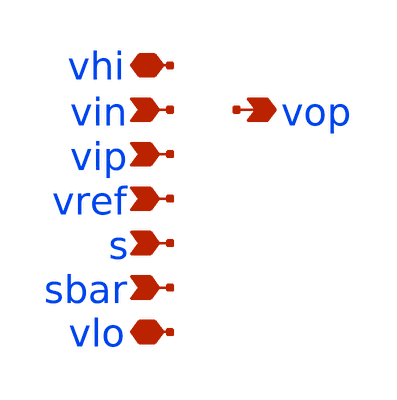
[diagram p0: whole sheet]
** sch_path: xschem/i_type_ota_gb_rp_gp_PEX.sch
**.subckt i_type_ota_gb_rp_gp_PEX vip vin vop vhi vlo vref s sbar
*.ipin vip
*.ipin vin
*.opin vop
*.iopin vhi
*.iopin vlo
*.ipin vref
*.ipin s
*.ipin sbar
**** begin user architecture code

* NGSPICE file created from cmota_1_flat.ext - technology: sky130A

.subckt cmota_gb_rp_gp VHI VLO VREF VIP VIN VOP S SBAR


X0 VLO a_n2179_n5512# a_n2179_n5512# VLO sky130_fd_pr__nfet_01v8 ad=0p pd=0u as=0p ps=0u w=1e+07u
+ l=300000u
X1 VLO VLO VLO VLO sky130_fd_pr__nfet_01v8 ad=0p pd=0u as=0p ps=0u w=1e+07u l=300000u
X2 a_n999_n4100# VIP a_n644_n3012# VLO sky130_fd_pr__nfet_01v8_lvt ad=0p pd=0u as=0p ps=0u
+ w=2.5e+06u l=150000u
X3 VLO VREF_GATED a_n999_n4100# VLO sky130_fd_pr__nfet_01v8 ad=0p pd=0u as=0p ps=0u w=1e+07u
+ l=2e+06u
X4 VREF_GATED S a_n3594_n6504# VLO sky130_fd_pr__nfet_01v8 ad=0p pd=0u as=0p ps=0u w=2.5e+06u
+ l=150000u
X5 VLO VREF_GATED a_n999_n4100# VLO sky130_fd_pr__nfet_01v8 ad=0p pd=0u as=0p ps=0u w=1e+07u
+ l=2e+06u
X6 a_n999_n4100# VIP a_n644_n3012# VLO sky130_fd_pr__nfet_01v8_lvt ad=0p pd=0u as=0p ps=0u
+ w=2.5e+06u l=150000u
X7 a_n3594_n6504# SBAR VLO VLO sky130_fd_pr__nfet_01v8 ad=0p pd=0u as=0p ps=0u w=2.5e+06u l=150000u
X8 VHI a_n644_n3012# VOP VHI sky130_fd_pr__pfet_01v8 ad=0p pd=0u as=0p ps=0u w=1e+07u l=300000u
X9 VLO VLO a_n999_n4100# VLO sky130_fd_pr__nfet_01v8_lvt ad=0p pd=0u as=0p ps=0u w=2.5e+06u
+ l=150000u
X10 VOP a_n644_n3012# VHI VHI sky130_fd_pr__pfet_01v8 ad=0p pd=0u as=0p ps=0u w=1e+07u l=300000u
X11 VLO VLO VLO VLO sky130_fd_pr__nfet_01v8_lvt ad=0p pd=0u as=0p ps=0u w=2.5e+06u l=150000u
X12 VLO VLO VLO VLO sky130_fd_pr__nfet_01v8 ad=0p pd=0u as=0p ps=0u w=1e+07u l=300000u
X13 VOP a_n2179_n5512# VLO VLO sky130_fd_pr__nfet_01v8 ad=0p pd=0u as=0p ps=0u w=1e+07u l=300000u
X14 VHI a_n644_n3012# VOP VHI sky130_fd_pr__pfet_01v8 ad=0p pd=0u as=0p ps=0u w=1e+07u l=300000u
X15 VLO a_n2179_n5512# VOP VLO sky130_fd_pr__nfet_01v8 ad=0p pd=0u as=0p ps=0u w=1e+07u l=300000u
X16 VLO VHI sky130_fd_pr__cap_mim_m3_2 l=3.1e+07u w=1.3e+07u
X17 VOP a_n644_n3012# VHI VHI sky130_fd_pr__pfet_01v8 ad=0p pd=0u as=0p ps=0u w=1e+07u l=300000u
X18 VLO a_n2179_n5512# a_n2179_n5512# VLO sky130_fd_pr__nfet_01v8 ad=0p pd=0u as=0p ps=0u w=1e+07u
+ l=300000u
X19 VHI a_n1942_n3012# a_n1942_n3012# VHI sky130_fd_pr__pfet_01v8 ad=0p pd=0u as=0p ps=0u w=1e+07u
+ l=300000u
X20 VLO VLO VLO VLO sky130_fd_pr__nfet_01v8 ad=0p pd=0u as=0p ps=0u w=1e+07u l=300000u
X21 a_n2179_n5512# a_n2179_n5512# VLO VLO sky130_fd_pr__nfet_01v8 ad=0p pd=0u as=0p ps=0u w=1e+07u
+ l=300000u
X22 VHI a_n1942_n3012# a_n1942_n3012# VHI sky130_fd_pr__pfet_01v8 ad=0p pd=0u as=0p ps=0u w=1e+07u
+ l=300000u
X23 a_n1942_n3012# a_n1942_n3012# VHI VHI sky130_fd_pr__pfet_01v8 ad=0p pd=0u as=0p ps=0u w=1e+07u
+ l=300000u
X24 a_n1942_n3012# VIN a_n999_n4100# VLO sky130_fd_pr__nfet_01v8_lvt ad=0p pd=0u as=0p ps=0u
+ w=2.5e+06u l=150000u
X25 a_127_n2915# a_n1942_n3012# VHI VHI sky130_fd_pr__pfet_01v8 ad=0p pd=0u as=0p ps=0u w=1e+07u
+ l=300000u
X26 a_n2179_n5512# a_n2179_n5512# VLO VLO sky130_fd_pr__nfet_01v8 ad=0p pd=0u as=0p ps=0u w=1e+07u
+ l=300000u
X27 a_n999_n4100# VIN a_n1942_n3012# VLO sky130_fd_pr__nfet_01v8_lvt ad=0p pd=0u as=0p ps=0u
+ w=2.5e+06u l=150000u
X28 a_n2179_n5512# a_n1942_n3012# VHI VHI sky130_fd_pr__pfet_01v8 ad=0p pd=0u as=0p ps=0u w=1e+07u
+ l=300000u
X29 VHI a_n1942_n3012# a_n2179_n5512# VHI sky130_fd_pr__pfet_01v8 ad=0p pd=0u as=0p ps=0u w=1e+07u
+ l=300000u
X30 a_n644_n3012# a_n644_n3012# VHI VHI sky130_fd_pr__pfet_01v8 ad=0p pd=0u as=0p ps=0u w=1e+07u
+ l=300000u
X31 VHI a_n644_n3012# a_n644_n3012# VHI sky130_fd_pr__pfet_01v8 ad=0p pd=0u as=0p ps=0u w=1e+07u
+ l=300000u
X32 a_n644_n3012# VIP a_n999_n4100# VLO sky130_fd_pr__nfet_01v8_lvt ad=0p pd=0u as=0p ps=0u
+ w=2.5e+06u l=150000u
X33 VLO VREF_GATED sky130_fd_pr__cap_mim_m3_1 l=2.7e+07u w=5.5e+06u
X34 a_n999_n4100# VIN a_n1942_n3012# VLO sky130_fd_pr__nfet_01v8_lvt ad=0p pd=0u as=0p ps=0u
+ w=2.5e+06u l=150000u
X35 a_n1942_n3012# VIN a_n999_n4100# VLO sky130_fd_pr__nfet_01v8_lvt ad=0p pd=0u as=0p ps=0u
+ w=2.5e+06u l=150000u
X36 VLO SBAR a_n3594_n6504# VLO sky130_fd_pr__nfet_01v8 ad=0p pd=0u as=0p ps=0u w=2.5e+06u l=150000u
X37 a_n644_n3012# VIP a_n999_n4100# VLO sky130_fd_pr__nfet_01v8_lvt ad=0p pd=0u as=0p ps=0u
+ w=2.5e+06u l=150000u
X38 a_n2179_n5512# VHI VHI VHI sky130_fd_pr__pfet_01v8 ad=0p pd=0u as=0p ps=0u w=1e+07u l=300000u
X39 VREF_GATED VLO sky130_fd_pr__cap_mim_m3_2 l=2.7e+07u w=5.5e+06u
X40 VHI a_n644_n3012# a_n1942_n3012# VHI sky130_fd_pr__pfet_01v8 ad=0p pd=0u as=0p ps=0u w=1e+07u
+ l=300000u
X41 a_n644_n3012# a_n1942_n3012# VHI VHI sky130_fd_pr__pfet_01v8 ad=0p pd=0u as=0p ps=0u w=1e+07u
+ l=300000u
X42 VHI a_n1942_n3012# a_n644_n3012# VHI sky130_fd_pr__pfet_01v8 ad=0p pd=0u as=0p ps=0u w=1e+07u
+ l=300000u
X43 VHI VHI VOP VHI sky130_fd_pr__pfet_01v8 ad=0p pd=0u as=0p ps=0u w=1e+07u l=300000u
X44 a_n999_n4100# VIP a_n644_n3012# VLO sky130_fd_pr__nfet_01v8_lvt ad=0p pd=0u as=0p ps=0u
+ w=2.5e+06u l=150000u
X45 VOP a_n2179_n5512# VLO VLO sky130_fd_pr__nfet_01v8 ad=0p pd=0u as=0p ps=0u w=1e+07u l=300000u
X46 VHI a_n1942_n3012# a_n2179_n5512# VHI sky130_fd_pr__pfet_01v8 ad=0p pd=0u as=0p ps=0u w=1e+07u
+ l=300000u
X47 a_n1942_n3012# a_n1942_n3012# VHI VHI sky130_fd_pr__pfet_01v8 ad=0p pd=0u as=0p ps=0u w=1e+07u
+ l=300000u
X48 a_n644_n3012# a_n644_n3012# VHI VHI sky130_fd_pr__pfet_01v8 ad=0p pd=0u as=0p ps=0u w=1e+07u
+ l=300000u
X49 VHI a_n1942_n3012# a_n2179_n5512# VHI sky130_fd_pr__pfet_01v8 ad=0p pd=0u as=0p ps=0u w=1e+07u
+ l=300000u
X50 VHI a_n644_n3012# a_n644_n3012# VHI sky130_fd_pr__pfet_01v8 ad=0p pd=0u as=0p ps=0u w=1e+07u
+ l=300000u
X51 a_n644_n3012# VIP a_n999_n4100# VLO sky130_fd_pr__nfet_01v8_lvt ad=0p pd=0u as=0p ps=0u
+ w=2.5e+06u l=150000u
X52 a_n3594_n6504# S VREF_GATED VLO sky130_fd_pr__nfet_01v8 ad=0p pd=0u as=0p ps=0u w=2.5e+06u
+ l=150000u
X53 VREF a_n3594_n6504# VLO sky130_fd_pr__res_xhigh_po w=350000u l=1.49e+06u
X54 a_n2179_n5512# a_2492_n4180# VLO sky130_fd_pr__res_high_po w=690000u l=5.83e+06u
X55 VOP a_n644_n3012# VHI VHI sky130_fd_pr__pfet_01v8 ad=0p pd=0u as=0p ps=0u w=1e+07u l=300000u
X56 VHI a_n644_n3012# VOP VHI sky130_fd_pr__pfet_01v8 ad=0p pd=0u as=0p ps=0u w=1e+07u l=300000u
X57 a_n999_n4100# VLO VLO VLO sky130_fd_pr__nfet_01v8_lvt ad=0p pd=0u as=0p ps=0u w=2.5e+06u
+ l=150000u
X58 a_n1942_n3012# VIN a_n999_n4100# VLO sky130_fd_pr__nfet_01v8_lvt ad=0p pd=0u as=0p ps=0u
+ w=2.5e+06u l=150000u
X59 a_n999_n4100# VREF_GATED VLO VLO sky130_fd_pr__nfet_01v8 ad=0p pd=0u as=0p ps=0u w=1e+07u
+ l=2e+06u
X60 VOP a_2492_n4180# sky130_fd_pr__cap_mim_m3_1 l=1.32e+07u w=3.7e+06u
X61 a_n644_n3012# VIP a_n999_n4100# VLO sky130_fd_pr__nfet_01v8_lvt ad=0p pd=0u as=0p ps=0u
+ w=2.5e+06u l=150000u
X62 VLO a_n2179_n5512# VOP VLO sky130_fd_pr__nfet_01v8 ad=0p pd=0u as=0p ps=0u w=1e+07u l=300000u
X63 VLO VLO VLO VLO sky130_fd_pr__nfet_01v8_lvt ad=0p pd=0u as=0p ps=0u w=2.5e+06u l=150000u
X64 a_n999_n4100# VIN a_n1942_n3012# VLO sky130_fd_pr__nfet_01v8_lvt ad=0p pd=0u as=0p ps=0u
+ w=2.5e+06u l=150000u
X65 VLO VLO VLO VLO sky130_fd_pr__nfet_01v8 ad=0p pd=0u as=0p ps=0u w=1e+07u l=300000u
X66 VOP a_n644_n3012# VHI VHI sky130_fd_pr__pfet_01v8 ad=0p pd=0u as=0p ps=0u w=1e+07u l=300000u
X67 a_n999_n4100# VIN a_n1942_n3012# VLO sky130_fd_pr__nfet_01v8_lvt ad=0p pd=0u as=0p ps=0u
+ w=2.5e+06u l=150000u
X68 VHI a_n1942_n3012# a_n2179_n5512# VHI sky130_fd_pr__pfet_01v8 ad=0p pd=0u as=0p ps=0u w=1e+07u
+ l=300000u
X69 a_n2179_n5512# a_n1942_n3012# VHI VHI sky130_fd_pr__pfet_01v8 ad=0p pd=0u as=0p ps=0u w=1e+07u
+ l=300000u
X70 a_n1942_n3012# a_n644_n3012# VHI VHI sky130_fd_pr__pfet_01v8 ad=0p pd=0u as=0p ps=0u w=1e+07u
+ l=300000u
X71 a_n1942_n3012# VIN a_n999_n4100# VLO sky130_fd_pr__nfet_01v8_lvt ad=0p pd=0u as=0p ps=0u
+ w=2.5e+06u l=150000u
X72 a_n999_n4100# VREF_GATED VLO VLO sky130_fd_pr__nfet_01v8 ad=0p pd=0u as=0p ps=0u w=1e+07u
+ l=2e+06u
X73 a_n2179_n5512# a_n1942_n3012# VHI VHI sky130_fd_pr__pfet_01v8 ad=0p pd=0u as=0p ps=0u w=1e+07u
+ l=300000u
X74 a_n581_n2915# a_n644_n3012# VHI VHI sky130_fd_pr__pfet_01v8 ad=0p pd=0u as=0p ps=0u w=1e+07u
+ l=300000u
X75 VHI a_n644_n3012# a_n581_n2915# VHI sky130_fd_pr__pfet_01v8 ad=0p pd=0u as=0p ps=0u w=1e+07u
+ l=300000u
X76 VHI a_n1942_n3012# a_127_n2915# VHI sky130_fd_pr__pfet_01v8 ad=0p pd=0u as=0p ps=0u w=1e+07u
+ l=300000u
X77 a_2492_n4180# VOP sky130_fd_pr__cap_mim_m3_2 l=1.32e+07u w=3.7e+06u
X78 a_n999_n4100# VIP a_n644_n3012# VLO sky130_fd_pr__nfet_01v8_lvt ad=0p pd=0u as=0p ps=0u
+ w=2.5e+06u l=150000u
X79 VHI VLO sky130_fd_pr__cap_mim_m3_1 l=3.1e+07u w=1.3e+07u
C0 VHI a_n2179_n5512# 17.90fF
C1 VREF_GATED VHI 4.82fF
C2 a_2492_n4180# VHI 2.09fF
C3 VHI a_n1942_n3012# 17.11fF
C4 VREF_GATED a_n999_n4100# 2.52fF
C5 VHI a_n581_n2915# 4.36fF
C6 a_2492_n4180# VOP 9.33fF
C7 a_n999_n4100# a_n1942_n3012# 6.05fF
C8 a_n644_n3012# VHI 17.03fF
C9 a_127_n2915# VHI 4.36fF
C10 VHI VOP 18.36fF
C11 a_n999_n4100# a_n644_n3012# 6.02fF
C12 a_2492_n4180# VLO 3.01fF $ **FLOATING
C13 VREF_GATED VLO 50.11fF $ **FLOATING
C14 a_n999_n4100# VLO 6.13fF $ **FLOATING
C15 VOP VLO 9.31fF $ **FLOATING
C16 a_n2179_n5512# VLO 14.00fF $ **FLOATING
C17 VHI VLO 113.86fF $ **FLOATING


.ends

XDUT vhi vlo vref vip vin vop s sbar cmota_gb_rp_gp


**** end user architecture code
**.ends
.end
